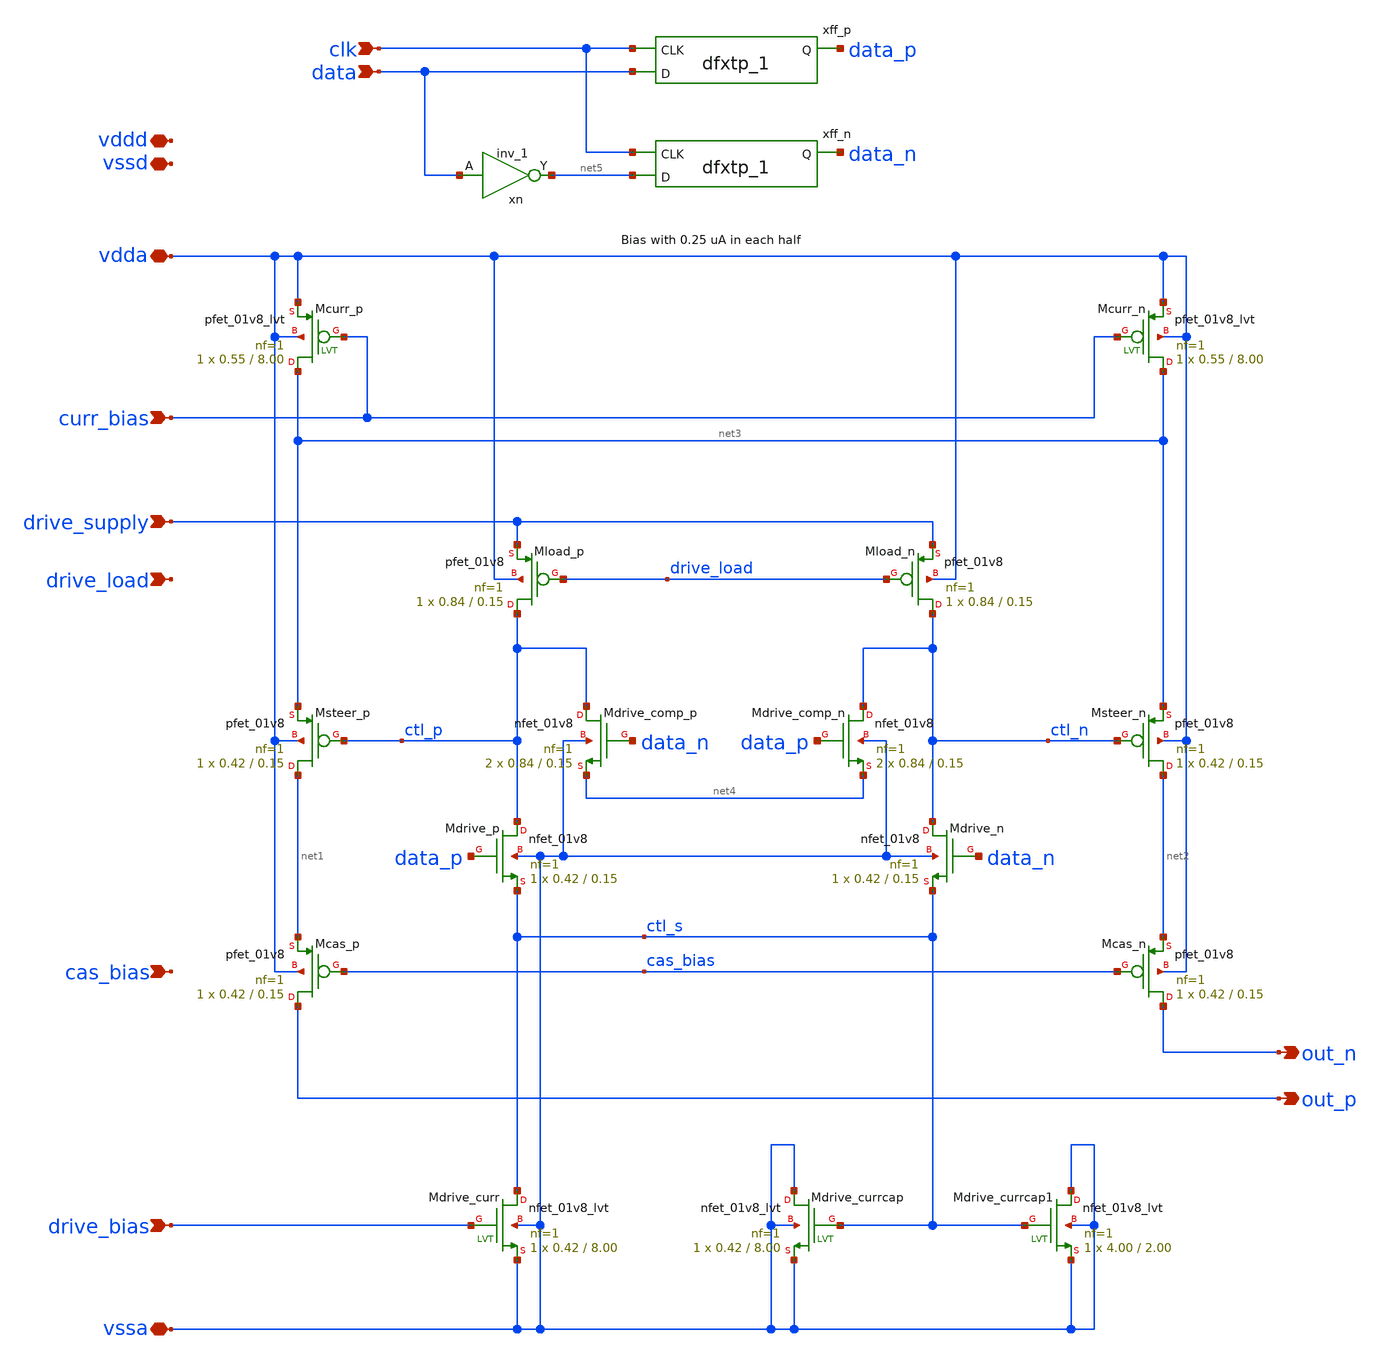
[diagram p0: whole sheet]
** sch_path: design/dac_unit_cell/dac_unit_cell.sch
**.subckt dac_unit_cell vdda vssa curr_bias clk data drive_supply out_p out_n cas_bias drive_bias
*+ drive_load vssd vddd
*.iopin vdda
*.iopin vssa
*.ipin curr_bias
*.ipin clk
*.ipin data
*.ipin drive_supply
*.opin out_p
*.opin out_n
*.ipin cas_bias
*.ipin drive_bias
*.ipin drive_load
*.iopin vssd
*.iopin vddd
XMcas_p out_p cas_bias net1 vdda sky130_fd_pr__pfet_01v8 L=0.15 W=0.42 nf=1 ad='W * 0.29' as='W * 0.29'
+ pd='2 * (W + 0.29)' ps='2 * (W + 0.29)' nrd='0.29 / W' nrs='0.29 / W' sa=0 sb=0 sd=0 mult=1 m=1
XMcas_n out_n cas_bias net2 vdda sky130_fd_pr__pfet_01v8 L=0.15 W=0.42 nf=1 ad='W * 0.29' as='W * 0.29'
+ pd='2 * (W + 0.29)' ps='2 * (W + 0.29)' nrd='0.29 / W' nrs='0.29 / W' sa=0 sb=0 sd=0 mult=1 m=1
XMcurr_p net3 curr_bias vdda vdda sky130_fd_pr__pfet_01v8_lvt L=8.00 W=0.55 nf=1 ad='int((nf+1)/2) * W/nf * 0.29'
+ as='int((nf+2)/2) * W/nf * 0.29' pd='2*int((nf+1)/2) * (W/nf + 0.29)' ps='2*int((nf+2)/2) * (W/nf + 0.29)'
+ nrd='0.29 / W' nrs='0.29 / W' sa=0 sb=0 sd=0 mult=1 m=1
XMcurr_n net3 curr_bias vdda vdda sky130_fd_pr__pfet_01v8_lvt L=8.00 W=0.55 nf=1 ad='int((nf+1)/2) * W/nf * 0.29'
+ as='int((nf+2)/2) * W/nf * 0.29' pd='2*int((nf+1)/2) * (W/nf + 0.29)' ps='2*int((nf+2)/2) * (W/nf + 0.29)'
+ nrd='0.29 / W' nrs='0.29 / W' sa=0 sb=0 sd=0 mult=1 m=1
XMsteer_p net1 ctl_p net3 vdda sky130_fd_pr__pfet_01v8 L=0.15 W=0.42 nf=1 ad='W * 0.29' as='W * 0.29'
+ pd='2 * (W + 0.29)' ps='2 * (W + 0.29)' nrd='0.29 / W' nrs='0.29 / W' sa=0 sb=0 sd=0 mult=1 m=1
XMsteer_n net2 ctl_n net3 vdda sky130_fd_pr__pfet_01v8 L=0.15 W=0.42 nf=1 ad='W * 0.29' as='W * 0.29'
+ pd='2 * (W + 0.29)' ps='2 * (W + 0.29)' nrd='0.29 / W' nrs='0.29 / W' sa=0 sb=0 sd=0 mult=1 m=1
XMdrive_p ctl_p data_p ctl_s vssa sky130_fd_pr__nfet_01v8 L=0.15 W=0.42 nf=1 ad='int((nf+1)/2) * W/nf * 0.29'
+ as='int((nf+2)/2) * W/nf * 0.29' pd='2*int((nf+1)/2) * (W/nf + 0.29)' ps='2*int((nf+2)/2) * (W/nf + 0.29)'
+ nrd='0.29 / W' nrs='0.29 / W' sa=0 sb=0 sd=0 mult=1 m=1
XMdrive_n ctl_n data_n ctl_s vssa sky130_fd_pr__nfet_01v8 L=0.15 W=0.42 nf=1 ad='int((nf+1)/2) * W/nf * 0.29'
+ as='int((nf+2)/2) * W/nf * 0.29' pd='2*int((nf+1)/2) * (W/nf + 0.29)' ps='2*int((nf+2)/2) * (W/nf + 0.29)'
+ nrd='0.29 / W' nrs='0.29 / W' sa=0 sb=0 sd=0 mult=1 m=1
XMdrive_comp_p ctl_p data_n net4 vssa sky130_fd_pr__nfet_01v8 L=0.15 W=0.84 nf=1 ad='int((nf+1)/2) * W/nf * 0.29'
+ as='int((nf+2)/2) * W/nf * 0.29' pd='2*int((nf+1)/2) * (W/nf + 0.29)' ps='2*int((nf+2)/2) * (W/nf + 0.29)'
+ nrd='0.29 / W' nrs='0.29 / W' sa=0 sb=0 sd=0 mult=2 m=2
XMdrive_comp_n ctl_n data_p net4 vssa sky130_fd_pr__nfet_01v8 L=0.15 W=0.84 nf=1 ad='int((nf+1)/2) * W/nf * 0.29'
+ as='int((nf+2)/2) * W/nf * 0.29' pd='2*int((nf+1)/2) * (W/nf + 0.29)' ps='2*int((nf+2)/2) * (W/nf + 0.29)'
+ nrd='0.29 / W' nrs='0.29 / W' sa=0 sb=0 sd=0 mult=2 m=2
xn data vssa vssa vddd vddd net5 sky130_fd_sc_hs__inv_1
xff_p clk data vssa vssa vddd vddd data_p sky130_fd_sc_hs__dfxtp_1
xff_n clk net5 vssa vssa vddd vddd data_n sky130_fd_sc_hs__dfxtp_1
XMload_p ctl_p drive_load drive_supply vdda sky130_fd_pr__pfet_01v8 L=0.15 W=0.84 nf=1 ad='W * 0.29'
+ as='W * 0.29' pd='2 * (W + 0.29)' ps='2 * (W + 0.29)' nrd='0.29 / W' nrs='0.29 / W' sa=0 sb=0 sd=0 mult=1
+ m=1
XMload_n ctl_n drive_load drive_supply vdda sky130_fd_pr__pfet_01v8 L=0.15 W=0.84 nf=1 ad='W * 0.29'
+ as='W * 0.29' pd='2 * (W + 0.29)' ps='2 * (W + 0.29)' nrd='0.29 / W' nrs='0.29 / W' sa=0 sb=0 sd=0 mult=1
+ m=1
XMdrive_curr ctl_s drive_bias vssa vssa sky130_fd_pr__nfet_01v8_lvt L=8.00 W=0.42 nf=1 ad='int((nf+1)/2) * W/nf * 0.29'
+ as='int((nf+2)/2) * W/nf * 0.29' pd='2*int((nf+1)/2) * (W/nf + 0.29)' ps='2*int((nf+2)/2) * (W/nf + 0.29)'
+ nrd='0.29 / W' nrs='0.29 / W' sa=0 sb=0 sd=0 mult=1 m=1
XMdrive_currcap vssa ctl_s vssa vssa sky130_fd_pr__nfet_01v8_lvt L=8.00 W=0.42 nf=1 ad='int((nf+1)/2) * W/nf * 0.29'
+ as='int((nf+2)/2) * W/nf * 0.29' pd='2*int((nf+1)/2) * (W/nf + 0.29)' ps='2*int((nf+2)/2) * (W/nf + 0.29)'
+ nrd='0.29 / W' nrs='0.29 / W' sa=0 sb=0 sd=0 mult=1 m=1
XMdrive_currcap1 vssa ctl_s vssa vssa sky130_fd_pr__nfet_01v8_lvt L=2.00 W=4.00 nf=1 ad='int((nf+1)/2) * W/nf * 0.29'
+ as='int((nf+2)/2) * W/nf * 0.29' pd='2*int((nf+1)/2) * (W/nf + 0.29)' ps='2*int((nf+2)/2) * (W/nf + 0.29)'
+ nrd='0.29 / W' nrs='0.29 / W' sa=0 sb=0 sd=0 mult=1 m=1
**.ends
.end
